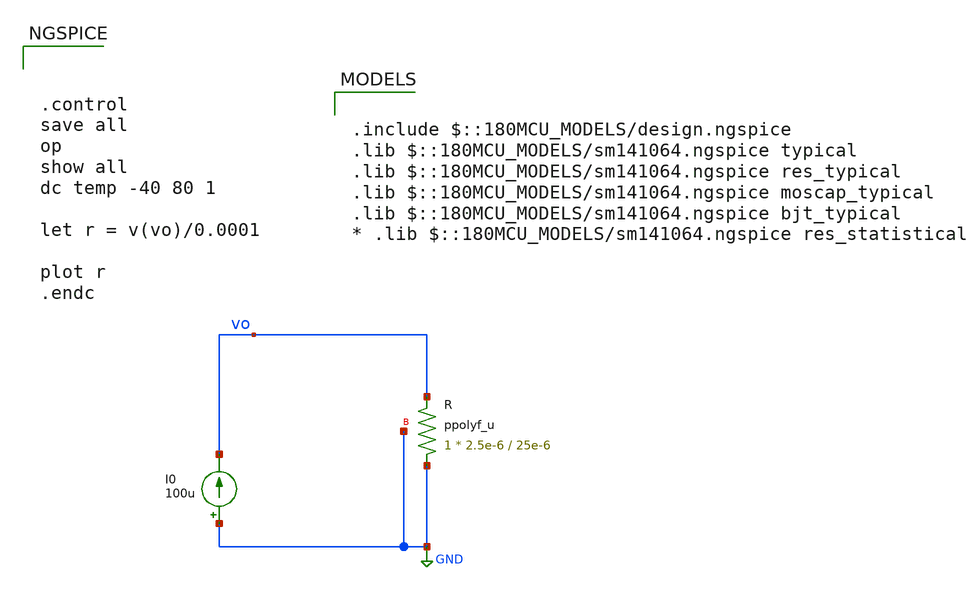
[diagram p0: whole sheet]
** sch_path: designs/libs/tb_analog_pads_pex/tech_resistors/p+_poly_unsalicided.sch
**.subckt p+_poly_unsalicided
I0 GND vo 100u
XR GND vo GND ppolyf_u r_width=2.5e-6 r_length=25e-6 m=1
**** begin user architecture code



.control
save all
op
show all
dc temp -40 80 1

let r = v(vo)/0.0001

plot r
.endc



.include $::180MCU_MODELS/design.ngspice
.lib $::180MCU_MODELS/sm141064.ngspice typical
.lib $::180MCU_MODELS/sm141064.ngspice res_typical
.lib $::180MCU_MODELS/sm141064.ngspice moscap_typical
.lib $::180MCU_MODELS/sm141064.ngspice bjt_typical
* .lib $::180MCU_MODELS/sm141064.ngspice res_statistical

**** end user architecture code
**.ends
.GLOBAL GND
.end
